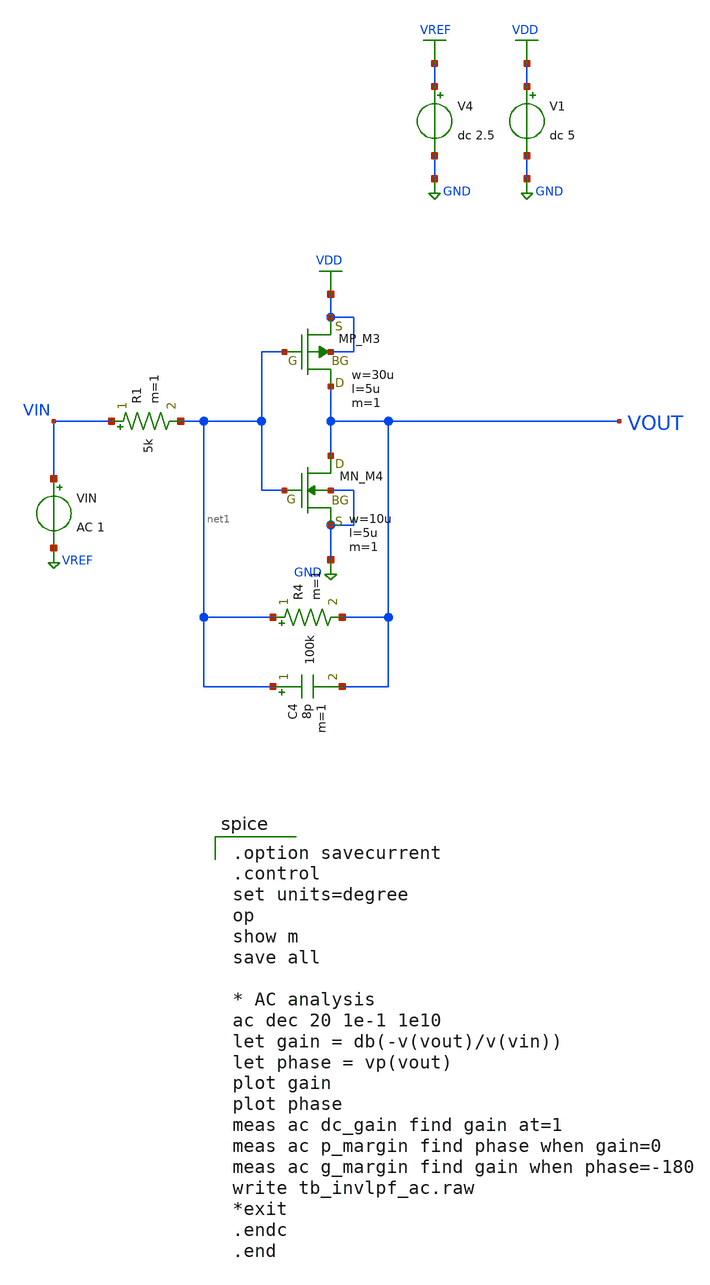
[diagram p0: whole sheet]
** sch_path: member_project/AM_Radio/Yamada3/xschem/tb_invlpf_ac.sch
**.subckt tb_invlpf_ac
VIN VIN VREF AC 1
V1 VDD GND dc 5
V4 VREF GND dc 2.5
XM3 VOUT net1 VDD VDD PMOS w=30u l=5u as=0 ad=0 ps=0 pd=0 nrd=0 nrs=0 m=1
XM4 VOUT net1 GND GND NMOS w=10u l=5u as=0 ad=0 ps=0 pd=0 nrd=0 nrs=0 m=1
R4 net1 VOUT 100k m=1
R1 VIN net1 5k m=1
C4 net1 VOUT 8p m=1
**** begin user architecture code

.option savecurrent
.control
set units=degree
op
show m
save all

* AC analysis
ac dec 20 1e-1 1e10
let gain = db(-v(vout)/v(vin))
let phase = vp(vout)
plot gain
plot phase
meas ac dc_gain find gain at=1
meas ac p_margin find phase when gain=0
meas ac g_margin find gain when phase=-180
write tb_invlpf_ac.raw
*exit
.endc
.end


 .include $::LIB/ip62_models
**** end user architecture code
**.ends
.GLOBAL VREF
.GLOBAL VDD
.GLOBAL GND
.end
